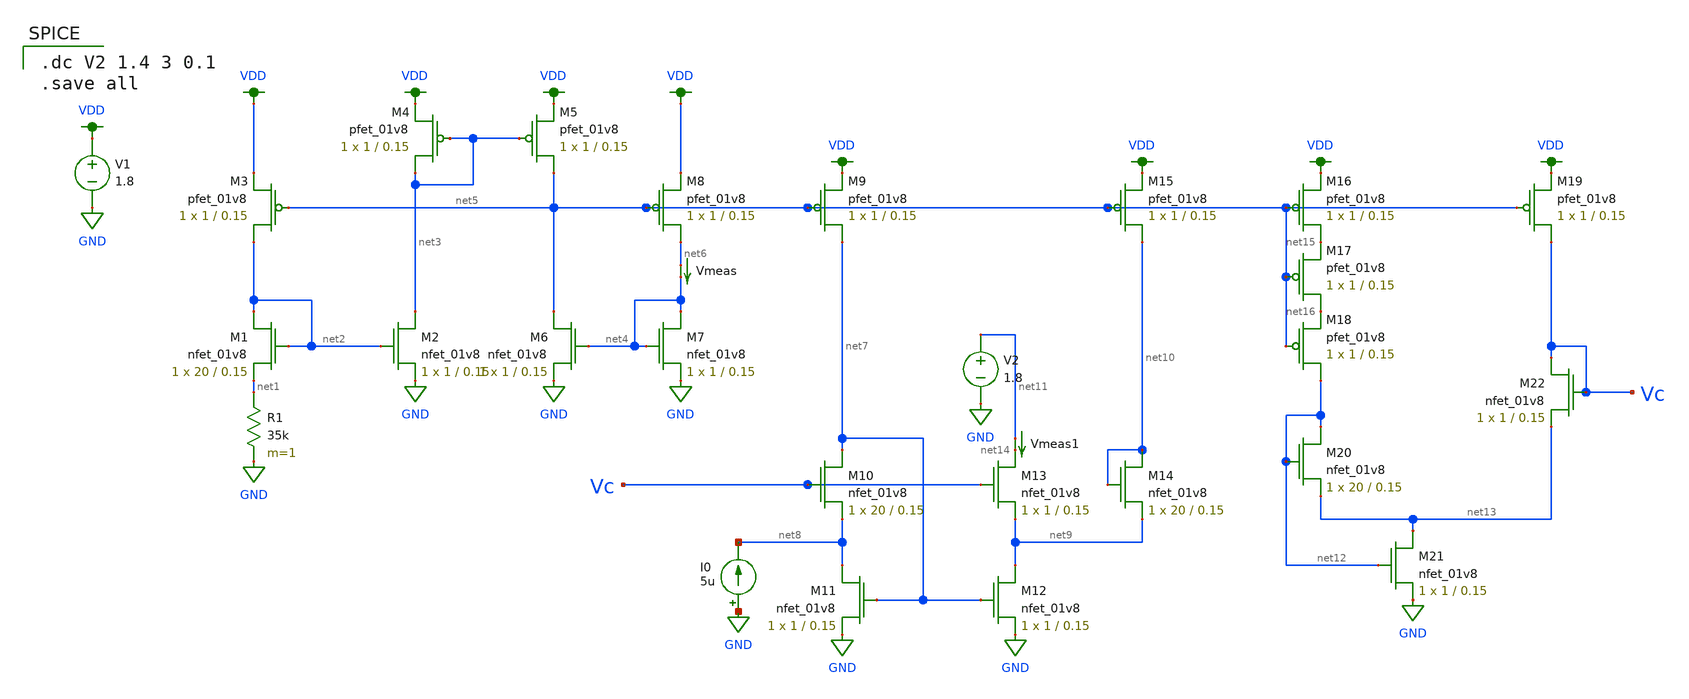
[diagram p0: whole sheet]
** sch_path: bootstrapbiasgen.sch
**.subckt bootstrapbiasgen
XM1 net2 net2 net1 GND sky130_fd_pr__nfet_01v8 L=0.15 W=20 nf=1 ad='int((nf+1)/2) * W/nf * 0.29' as='int((nf+2)/2) * W/nf * 0.29'
+ pd='2*int((nf+1)/2) * (W/nf + 0.29)' ps='2*int((nf+2)/2) * (W/nf + 0.29)' nrd='0.29 / W' nrs='0.29 / W'
+ sa=0 sb=0 sd=0 mult=1 m=1
XM2 net3 net2 GND GND sky130_fd_pr__nfet_01v8 L=0.15 W=1 nf=1 ad='int((nf+1)/2) * W/nf * 0.29' as='int((nf+2)/2) * W/nf * 0.29'
+ pd='2*int((nf+1)/2) * (W/nf + 0.29)' ps='2*int((nf+2)/2) * (W/nf + 0.29)' nrd='0.29 / W' nrs='0.29 / W'
+ sa=0 sb=0 sd=0 mult=1 m=1
R1 net1 GND 35k m=1
XM3 net2 net5 VDD VDD sky130_fd_pr__pfet_01v8 L=0.15 W=1 nf=1 ad='int((nf+1)/2) * W/nf * 0.29' as='int((nf+2)/2) * W/nf * 0.29'
+ pd='2*int((nf+1)/2) * (W/nf + 0.29)' ps='2*int((nf+2)/2) * (W/nf + 0.29)' nrd='0.29 / W' nrs='0.29 / W'
+ sa=0 sb=0 sd=0 mult=1 m=1
XM4 net3 net3 VDD VDD sky130_fd_pr__pfet_01v8 L=0.15 W=1 nf=1 ad='int((nf+1)/2) * W/nf * 0.29' as='int((nf+2)/2) * W/nf * 0.29'
+ pd='2*int((nf+1)/2) * (W/nf + 0.29)' ps='2*int((nf+2)/2) * (W/nf + 0.29)' nrd='0.29 / W' nrs='0.29 / W'
+ sa=0 sb=0 sd=0 mult=1 m=1
XM5 net5 net3 VDD VDD sky130_fd_pr__pfet_01v8 L=0.15 W=1 nf=1 ad='int((nf+1)/2) * W/nf * 0.29' as='int((nf+2)/2) * W/nf * 0.29'
+ pd='2*int((nf+1)/2) * (W/nf + 0.29)' ps='2*int((nf+2)/2) * (W/nf + 0.29)' nrd='0.29 / W' nrs='0.29 / W'
+ sa=0 sb=0 sd=0 mult=1 m=1
XM6 net5 net4 GND GND sky130_fd_pr__nfet_01v8 L=0.15 W=1 nf=1 ad='int((nf+1)/2) * W/nf * 0.29' as='int((nf+2)/2) * W/nf * 0.29'
+ pd='2*int((nf+1)/2) * (W/nf + 0.29)' ps='2*int((nf+2)/2) * (W/nf + 0.29)' nrd='0.29 / W' nrs='0.29 / W'
+ sa=0 sb=0 sd=0 mult=1 m=1
XM7 net4 net4 GND GND sky130_fd_pr__nfet_01v8 L=0.15 W=1 nf=1 ad='int((nf+1)/2) * W/nf * 0.29' as='int((nf+2)/2) * W/nf * 0.29'
+ pd='2*int((nf+1)/2) * (W/nf + 0.29)' ps='2*int((nf+2)/2) * (W/nf + 0.29)' nrd='0.29 / W' nrs='0.29 / W'
+ sa=0 sb=0 sd=0 mult=1 m=1
XM8 net6 net5 VDD VDD sky130_fd_pr__pfet_01v8 L=0.15 W=1 nf=1 ad='int((nf+1)/2) * W/nf * 0.29' as='int((nf+2)/2) * W/nf * 0.29'
+ pd='2*int((nf+1)/2) * (W/nf + 0.29)' ps='2*int((nf+2)/2) * (W/nf + 0.29)' nrd='0.29 / W' nrs='0.29 / W'
+ sa=0 sb=0 sd=0 mult=1 m=1
V1 VDD GND 1.8
Vmeas net6 net4 0
.save i(vmeas)
XM9 net7 net5 VDD VDD sky130_fd_pr__pfet_01v8 L=0.15 W=1 nf=1 ad='int((nf+1)/2) * W/nf * 0.29' as='int((nf+2)/2) * W/nf * 0.29'
+ pd='2*int((nf+1)/2) * (W/nf + 0.29)' ps='2*int((nf+2)/2) * (W/nf + 0.29)' nrd='0.29 / W' nrs='0.29 / W'
+ sa=0 sb=0 sd=0 mult=1 m=1
XM10 net7 Vc net8 GND sky130_fd_pr__nfet_01v8 L=0.15 W=20 nf=1 ad='int((nf+1)/2) * W/nf * 0.29' as='int((nf+2)/2) * W/nf * 0.29'
+ pd='2*int((nf+1)/2) * (W/nf + 0.29)' ps='2*int((nf+2)/2) * (W/nf + 0.29)' nrd='0.29 / W' nrs='0.29 / W'
+ sa=0 sb=0 sd=0 mult=1 m=1
XM11 net8 net7 GND GND sky130_fd_pr__nfet_01v8 L=0.15 W=1 nf=1 ad='int((nf+1)/2) * W/nf * 0.29' as='int((nf+2)/2) * W/nf * 0.29'
+ pd='2*int((nf+1)/2) * (W/nf + 0.29)' ps='2*int((nf+2)/2) * (W/nf + 0.29)' nrd='0.29 / W' nrs='0.29 / W'
+ sa=0 sb=0 sd=0 mult=1 m=1
I0 GND net8 5u
XM12 net9 net7 GND GND sky130_fd_pr__nfet_01v8 L=0.15 W=1 nf=1 ad='int((nf+1)/2) * W/nf * 0.29' as='int((nf+2)/2) * W/nf * 0.29'
+ pd='2*int((nf+1)/2) * (W/nf + 0.29)' ps='2*int((nf+2)/2) * (W/nf + 0.29)' nrd='0.29 / W' nrs='0.29 / W'
+ sa=0 sb=0 sd=0 mult=1 m=1
XM13 net14 Vc net9 GND sky130_fd_pr__nfet_01v8 L=0.15 W=1 nf=1 ad='int((nf+1)/2) * W/nf * 0.29' as='int((nf+2)/2) * W/nf * 0.29'
+ pd='2*int((nf+1)/2) * (W/nf + 0.29)' ps='2*int((nf+2)/2) * (W/nf + 0.29)' nrd='0.29 / W' nrs='0.29 / W'
+ sa=0 sb=0 sd=0 mult=1 m=1
XM14 net10 net10 net9 GND sky130_fd_pr__nfet_01v8 L=0.15 W=20 nf=1 ad='int((nf+1)/2) * W/nf * 0.29' as='int((nf+2)/2) * W/nf * 0.29'
+ pd='2*int((nf+1)/2) * (W/nf + 0.29)' ps='2*int((nf+2)/2) * (W/nf + 0.29)' nrd='0.29 / W' nrs='0.29 / W'
+ sa=0 sb=0 sd=0 mult=1 m=1
XM15 net10 net5 VDD VDD sky130_fd_pr__pfet_01v8 L=0.15 W=1 nf=1 ad='int((nf+1)/2) * W/nf * 0.29' as='int((nf+2)/2) * W/nf * 0.29'
+ pd='2*int((nf+1)/2) * (W/nf + 0.29)' ps='2*int((nf+2)/2) * (W/nf + 0.29)' nrd='0.29 / W' nrs='0.29 / W'
+ sa=0 sb=0 sd=0 mult=1 m=1
Vmeas1 net11 net14 0
.save i(vmeas1)
V2 net11 GND 1.8
XM16 net15 net5 VDD VDD sky130_fd_pr__pfet_01v8 L=0.15 W=1 nf=1 ad='int((nf+1)/2) * W/nf * 0.29' as='int((nf+2)/2) * W/nf * 0.29'
+ pd='2*int((nf+1)/2) * (W/nf + 0.29)' ps='2*int((nf+2)/2) * (W/nf + 0.29)' nrd='0.29 / W' nrs='0.29 / W'
+ sa=0 sb=0 sd=0 mult=1 m=1
XM17 net16 net5 net15 VDD sky130_fd_pr__pfet_01v8 L=0.15 W=1 nf=1 ad='int((nf+1)/2) * W/nf * 0.29' as='int((nf+2)/2) * W/nf * 0.29'
+ pd='2*int((nf+1)/2) * (W/nf + 0.29)' ps='2*int((nf+2)/2) * (W/nf + 0.29)' nrd='0.29 / W' nrs='0.29 / W'
+ sa=0 sb=0 sd=0 mult=1 m=1
XM18 net12 net5 net16 VDD sky130_fd_pr__pfet_01v8 L=0.15 W=1 nf=1 ad='int((nf+1)/2) * W/nf * 0.29' as='int((nf+2)/2) * W/nf * 0.29'
+ pd='2*int((nf+1)/2) * (W/nf + 0.29)' ps='2*int((nf+2)/2) * (W/nf + 0.29)' nrd='0.29 / W' nrs='0.29 / W'
+ sa=0 sb=0 sd=0 mult=1 m=1
XM19 Vc net5 VDD VDD sky130_fd_pr__pfet_01v8 L=0.15 W=1 nf=1 ad='int((nf+1)/2) * W/nf * 0.29' as='int((nf+2)/2) * W/nf * 0.29'
+ pd='2*int((nf+1)/2) * (W/nf + 0.29)' ps='2*int((nf+2)/2) * (W/nf + 0.29)' nrd='0.29 / W' nrs='0.29 / W'
+ sa=0 sb=0 sd=0 mult=1 m=1
XM20 net12 net12 net13 GND sky130_fd_pr__nfet_01v8 L=0.15 W=20 nf=1 ad='int((nf+1)/2) * W/nf * 0.29'
+ as='int((nf+2)/2) * W/nf * 0.29' pd='2*int((nf+1)/2) * (W/nf + 0.29)' ps='2*int((nf+2)/2) * (W/nf + 0.29)'
+ nrd='0.29 / W' nrs='0.29 / W' sa=0 sb=0 sd=0 mult=1 m=1
XM21 net13 net12 GND GND sky130_fd_pr__nfet_01v8 L=0.15 W=1 nf=1 ad='int((nf+1)/2) * W/nf * 0.29' as='int((nf+2)/2) * W/nf * 0.29'
+ pd='2*int((nf+1)/2) * (W/nf + 0.29)' ps='2*int((nf+2)/2) * (W/nf + 0.29)' nrd='0.29 / W' nrs='0.29 / W'
+ sa=0 sb=0 sd=0 mult=1 m=1
XM22 Vc Vc net13 GND sky130_fd_pr__nfet_01v8 L=0.15 W=1 nf=1 ad='int((nf+1)/2) * W/nf * 0.29' as='int((nf+2)/2) * W/nf * 0.29'
+ pd='2*int((nf+1)/2) * (W/nf + 0.29)' ps='2*int((nf+2)/2) * (W/nf + 0.29)' nrd='0.29 / W' nrs='0.29 / W'
+ sa=0 sb=0 sd=0 mult=1 m=1
**** begin user architecture code

.dc V2 1.4 3 0.1
.save all


.lib $::SKYWATER_MODELS/sky130.lib.spice ff

**** end user architecture code
**.ends
.GLOBAL GND
.GLOBAL VDD
.end
